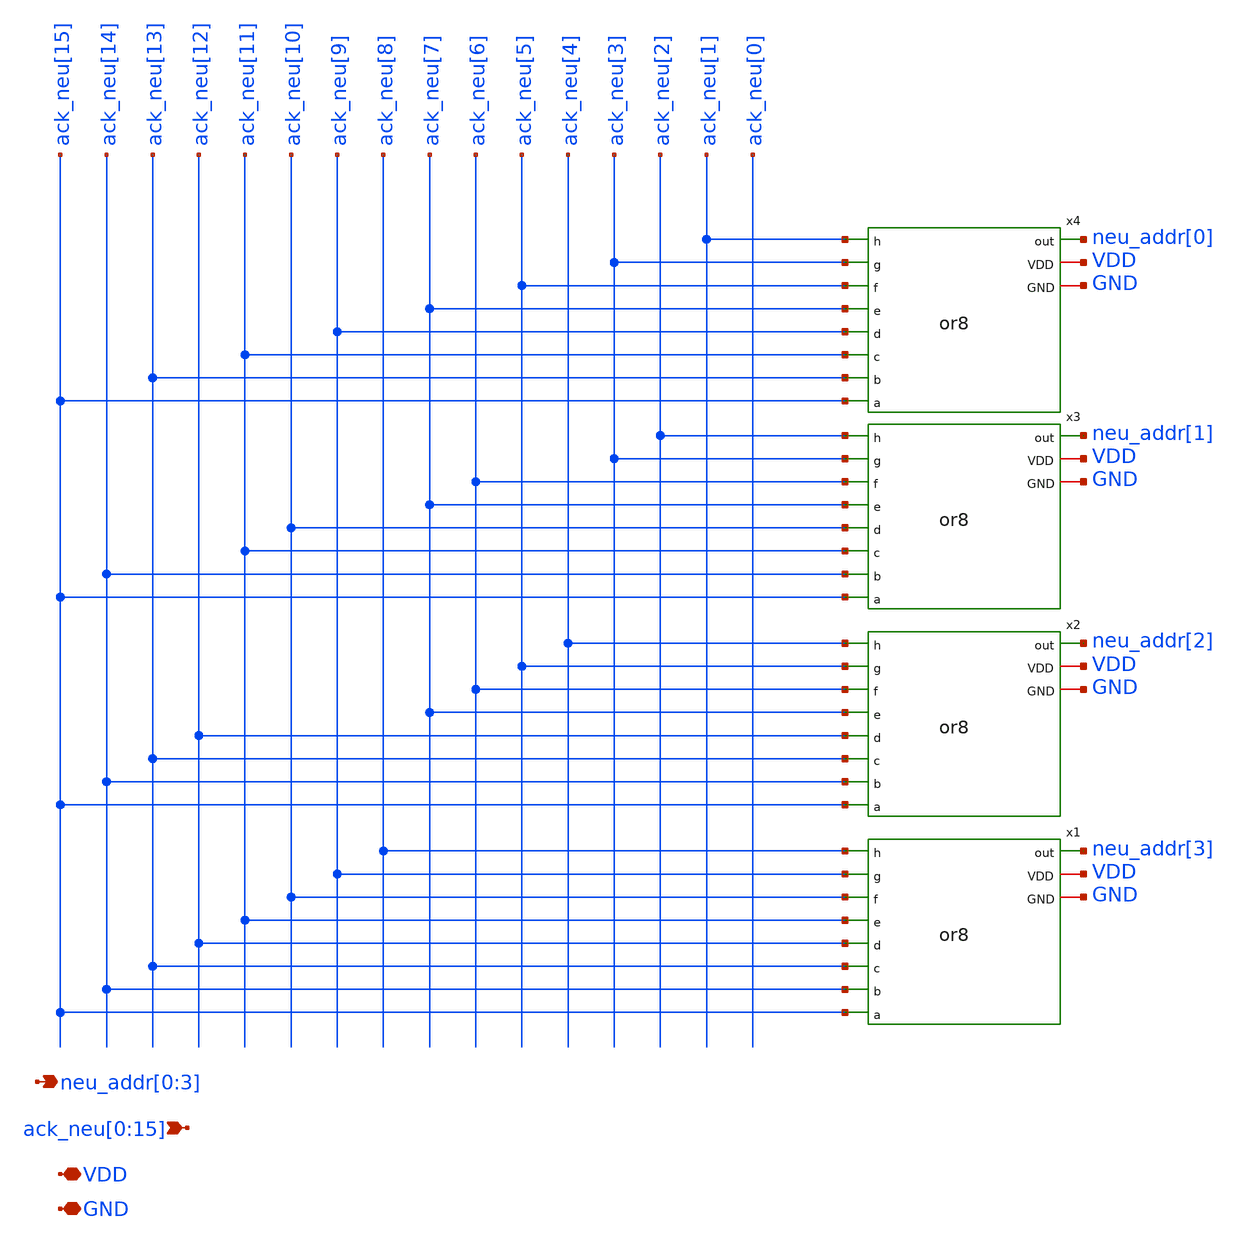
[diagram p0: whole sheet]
** sch_path: design/xschem/encoder_16_to_4.sch
**.subckt encoder_16_to_4 neu_addr[0],neu_addr[1],neu_addr[2],neu_addr[3]
*+ ack_neu[0],ack_neu[1],ack_neu[2],ack_neu[3],ack_neu[4],ack_neu[5],ack_neu[6],ack_neu[7],ack_neu[8],ack_neu[9],ack_neu[10],ack_neu[11],ack_neu[12],ack_neu[13],ack_neu[14],ack_neu[15] VDD GND
*.opin neu_addr[0],neu_addr[1],neu_addr[2],neu_addr[3]
*.ipin
*+ ack_neu[0],ack_neu[1],ack_neu[2],ack_neu[3],ack_neu[4],ack_neu[5],ack_neu[6],ack_neu[7],ack_neu[8],ack_neu[9],ack_neu[10],ack_neu[11],ack_neu[12],ack_neu[13],ack_neu[14],ack_neu[15]
*.iopin VDD
*.iopin GND
x1 ack_neu[8] ack_neu[9] ack_neu[10] ack_neu[11] neu_addr[3] ack_neu[12] ack_neu[13] ack_neu[14]
+ ack_neu[15] VDD GND or8
x2 ack_neu[4] ack_neu[5] ack_neu[6] ack_neu[7] neu_addr[2] ack_neu[12] ack_neu[13] ack_neu[14]
+ ack_neu[15] VDD GND or8
x3 ack_neu[2] ack_neu[3] ack_neu[6] ack_neu[7] neu_addr[1] ack_neu[10] ack_neu[11] ack_neu[14]
+ ack_neu[15] VDD GND or8
x4 ack_neu[1] ack_neu[3] ack_neu[5] ack_neu[7] neu_addr[0] ack_neu[9] ack_neu[11] ack_neu[13]
+ ack_neu[15] VDD GND or8
**.ends

* expanding   symbol:  or8.sym # of pins=11
** sym_path: design/xschem/or8.sym
** sch_path: design/xschem/or8.sch
.subckt or8 h g f e out d c b a VDD GND
*.ipin a
*.ipin b
*.ipin c
*.ipin d
*.ipin e
*.ipin f
*.ipin g
*.ipin h
*.opin out
*.iopin VDD
*.iopin GND
x1 h g f e GND GND VDD VDD net1 sky130_fd_sc_hd__or4_1
x2 d c b a GND GND VDD VDD net2 sky130_fd_sc_hd__or4_1
x3 net1 net2 GND GND VDD VDD out sky130_fd_sc_hd__or2_1
.ends

.end
